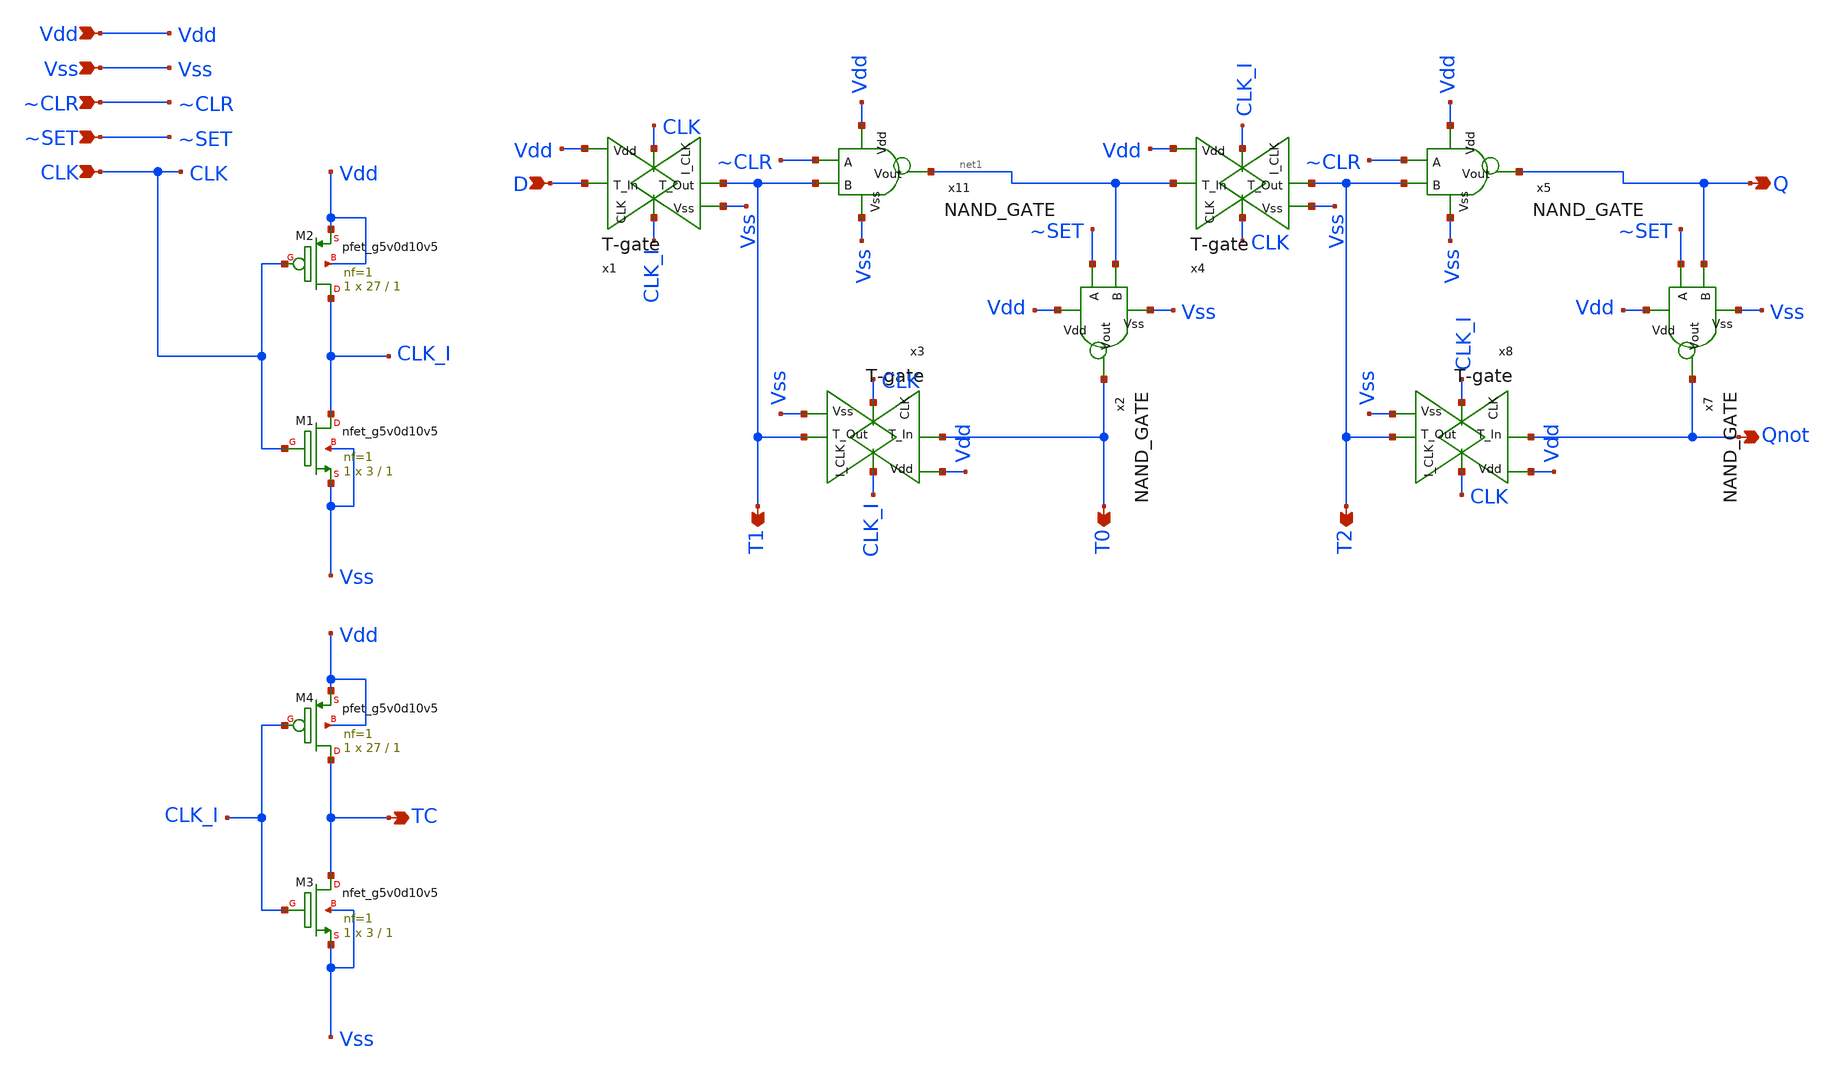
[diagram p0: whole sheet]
** sch_path: xschem/D-Edge.sch
**.subckt D-Edge D Vdd Vss Q Qnot ~CLR ~SET CLK T0 T1 T2 TC
*.ipin D
*.ipin Vdd
*.ipin Vss
*.opin Q
*.opin Qnot
*.ipin ~CLR
*.ipin ~SET
*.ipin CLK
*.opin T0
*.opin T1
*.opin T2
*.opin TC
x1 CLK D T1 Vdd Vss CLK_I T-gate
x3 CLK_I T0 T1 Vdd Vss CLK T-gate
x4 CLK_I net1 T2 Vdd Vss CLK T-gate
x8 CLK Qnot T2 Vdd Vss CLK_I T-gate
x11 Vdd ~CLR T1 net1 Vss NAND_GATE
x2 Vdd ~SET net1 T0 Vss NAND_GATE
x5 Vdd ~CLR T2 Q Vss NAND_GATE
x7 Vdd ~SET Q Qnot Vss NAND_GATE
XM1 CLK_I CLK Vss Vss sky130_fd_pr__nfet_g5v0d10v5 L=1 W=3 nf=1 ad='int((1 + 1)/2) * 3 / 1 * 0.29' as='int((1 + 2)/2) * 3 / 1 * 0.29'
+ pd='2*int((1 + 1)/2) * (3 / 1 + 0.29)' ps='2*int((1 + 2)/2) * (3 / 1 + 0.29)' nrd='0.29 / 3 ' nrs='0.29 / 3 '
+ sa=0 sb=0 sd=0 mult=1 m=1
XM2 CLK_I CLK Vdd Vdd sky130_fd_pr__pfet_g5v0d10v5 L=1 W=27 nf=1 ad='int((1 + 1)/2) * 27 / 1 * 0.29'
+ as='int((1 + 2)/2) * 27 / 1 * 0.29' pd='2*int((1 + 1)/2) * (27 / 1 + 0.29)' ps='2*int((1 + 2)/2) * (27 / 1 + 0.29)'
+ nrd='0.29 / 27 ' nrs='0.29 / 27 ' sa=0 sb=0 sd=0 mult=1 m=1
XM3 TC CLK_I Vss Vss sky130_fd_pr__nfet_g5v0d10v5 L=1 W=3 nf=1 ad='int((1 + 1)/2) * 3 / 1 * 0.29' as='int((1 + 2)/2) * 3 / 1 * 0.29'
+ pd='2*int((1 + 1)/2) * (3 / 1 + 0.29)' ps='2*int((1 + 2)/2) * (3 / 1 + 0.29)' nrd='0.29 / 3 ' nrs='0.29 / 3 '
+ sa=0 sb=0 sd=0 mult=1 m=1
XM4 TC CLK_I Vdd Vdd sky130_fd_pr__pfet_g5v0d10v5 L=1 W=27 nf=1 ad='int((1 + 1)/2) * 27 / 1 * 0.29' as='int((1 + 2)/2) * 27 / 1 * 0.29'
+ pd='2*int((1 + 1)/2) * (27 / 1 + 0.29)' ps='2*int((1 + 2)/2) * (27 / 1 + 0.29)' nrd='0.29 / 27 ' nrs='0.29 / 27 '
+ sa=0 sb=0 sd=0 mult=1 m=1
**.ends

* expanding   symbol:  T-gate.sym # of pins=6
** sym_path: xschem/T-gate.sym
** sch_path: xschem/T-gate.sch
.subckt T-gate I_CLK T_In T_Out Vdd Vss CLK
*.ipin T_In
*.opin T_Out
*.ipin Vdd
*.ipin Vss
*.ipin I_CLK
*.ipin CLK
XM1 T_In I_CLK T_Out Vdd sky130_fd_pr__pfet_g5v0d10v5 L=0.5 W=3 nf=1 ad='int((1 + 1)/2) * 3 / 1 * 0.29'
+ as='int((1 + 2)/2) * 3 / 1 * 0.29' pd='2*int((1 + 1)/2) * (3 / 1 + 0.29)' ps='2*int((1 + 2)/2) * (3 / 1 + 0.29)'
+ nrd='0.29 / 3 ' nrs='0.29 / 3 ' sa=0 sb=0 sd=0 mult=1 m=1
XM3 T_Out CLK T_In Vss sky130_fd_pr__nfet_g5v0d10v5 L=0.5 W=1 nf=1 ad='int((1 + 1)/2) * 1 / 1 * 0.29'
+ as='int((1 + 2)/2) * 1 / 1 * 0.29' pd='2*int((1 + 1)/2) * (1 / 1 + 0.29)' ps='2*int((1 + 2)/2) * (1 / 1 + 0.29)'
+ nrd='0.29 / 1 ' nrs='0.29 / 1 ' sa=0 sb=0 sd=0 mult=1 m=1
XM2 T_Out CLK T_Out Vdd sky130_fd_pr__pfet_g5v0d10v5 L=0.5 W=1.5 nf=1 ad='int((1 + 1)/2) * 1.5 / 1 * 0.29'
+ as='int((1 + 2)/2) * 1.5 / 1 * 0.29' pd='2*int((1 + 1)/2) * (1.5 / 1 + 0.29)' ps='2*int((1 + 2)/2) * (1.5 / 1 + 0.29)'
+ nrd='0.29 / 1.5 ' nrs='0.29 / 1.5 ' sa=0 sb=0 sd=0 mult=1 m=1
XM4 T_In CLK T_In Vdd sky130_fd_pr__pfet_g5v0d10v5 L=0.5 W=1.5 nf=1 ad='int((1 + 1)/2) * 1.5 / 1 * 0.29'
+ as='int((1 + 2)/2) * 1.5 / 1 * 0.29' pd='2*int((1 + 1)/2) * (1.5 / 1 + 0.29)' ps='2*int((1 + 2)/2) * (1.5 / 1 + 0.29)'
+ nrd='0.29 / 1.5 ' nrs='0.29 / 1.5 ' sa=0 sb=0 sd=0 mult=1 m=1
XM5 T_In I_CLK T_In Vss sky130_fd_pr__nfet_g5v0d10v5 L=0.5 W=0.5 nf=1 ad='int((1 + 1)/2) * 0.5 / 1 * 0.29'
+ as='int((1 + 2)/2) * 0.5 / 1 * 0.29' pd='2*int((1 + 1)/2) * (0.5 / 1 + 0.29)' ps='2*int((1 + 2)/2) * (0.5 / 1 + 0.29)'
+ nrd='0.29 / 0.5 ' nrs='0.29 / 0.5 ' sa=0 sb=0 sd=0 mult=1 m=1
XM6 T_Out I_CLK T_Out Vss sky130_fd_pr__nfet_g5v0d10v5 L=0.5 W=0.5 nf=1 ad='int((1 + 1)/2) * 0.5 / 1 * 0.29'
+ as='int((1 + 2)/2) * 0.5 / 1 * 0.29' pd='2*int((1 + 1)/2) * (0.5 / 1 + 0.29)' ps='2*int((1 + 2)/2) * (0.5 / 1 + 0.29)'
+ nrd='0.29 / 0.5 ' nrs='0.29 / 0.5 ' sa=0 sb=0 sd=0 mult=1 m=1
.ends


* expanding   symbol:  NAND_GATE.sym # of pins=5
** sym_path: xschem/NAND_GATE.sym
** sch_path: xschem/NAND_GATE.sch
.subckt NAND_GATE Vdd A B Vout Vss
*.ipin Vdd
*.ipin Vss
*.ipin A
*.ipin B
*.opin Vout
XM3 Vout A net1 Vss sky130_fd_pr__nfet_g5v0d10v5 L=0.5 W=1 nf=1 ad='int((1 + 1)/2) * 1 / 1 * 0.29' as='int((1 + 2)/2) * 1 / 1 * 0.29'
+ pd='2*int((1 + 1)/2) * (1 / 1 + 0.29)' ps='2*int((1 + 2)/2) * (1 / 1 + 0.29)' nrd='0.29 / 1 ' nrs='0.29 / 1 '
+ sa=0 sb=0 sd=0 mult=1 m=1
XM4 Vout A Vdd Vdd sky130_fd_pr__pfet_g5v0d10v5 L=0.5 W=3 nf=1 ad='int((1 + 1)/2) * 3 / 1 * 0.29' as='int((1 + 2)/2) * 3 / 1 * 0.29'
+ pd='2*int((1 + 1)/2) * (3 / 1 + 0.29)' ps='2*int((1 + 2)/2) * (3 / 1 + 0.29)' nrd='0.29 / 3 ' nrs='0.29 / 3 '
+ sa=0 sb=0 sd=0 mult=1 m=1
XM5 Vout B Vdd Vdd sky130_fd_pr__pfet_g5v0d10v5 L=0.5 W=3 nf=1 ad='int((1 + 1)/2) * 3 / 1 * 0.29' as='int((1 + 2)/2) * 3 / 1 * 0.29'
+ pd='2*int((1 + 1)/2) * (3 / 1 + 0.29)' ps='2*int((1 + 2)/2) * (3 / 1 + 0.29)' nrd='0.29 / 3 ' nrs='0.29 / 3 '
+ sa=0 sb=0 sd=0 mult=1 m=1
XM1 net1 B Vss Vss sky130_fd_pr__nfet_g5v0d10v5 L=0.5 W=1 nf=1 ad='int((1 + 1)/2) * 1 / 1 * 0.29' as='int((1 + 2)/2) * 1 / 1 * 0.29'
+ pd='2*int((1 + 1)/2) * (1 / 1 + 0.29)' ps='2*int((1 + 2)/2) * (1 / 1 + 0.29)' nrd='0.29 / 1 ' nrs='0.29 / 1 '
+ sa=0 sb=0 sd=0 mult=1 m=1
.ends

.end
